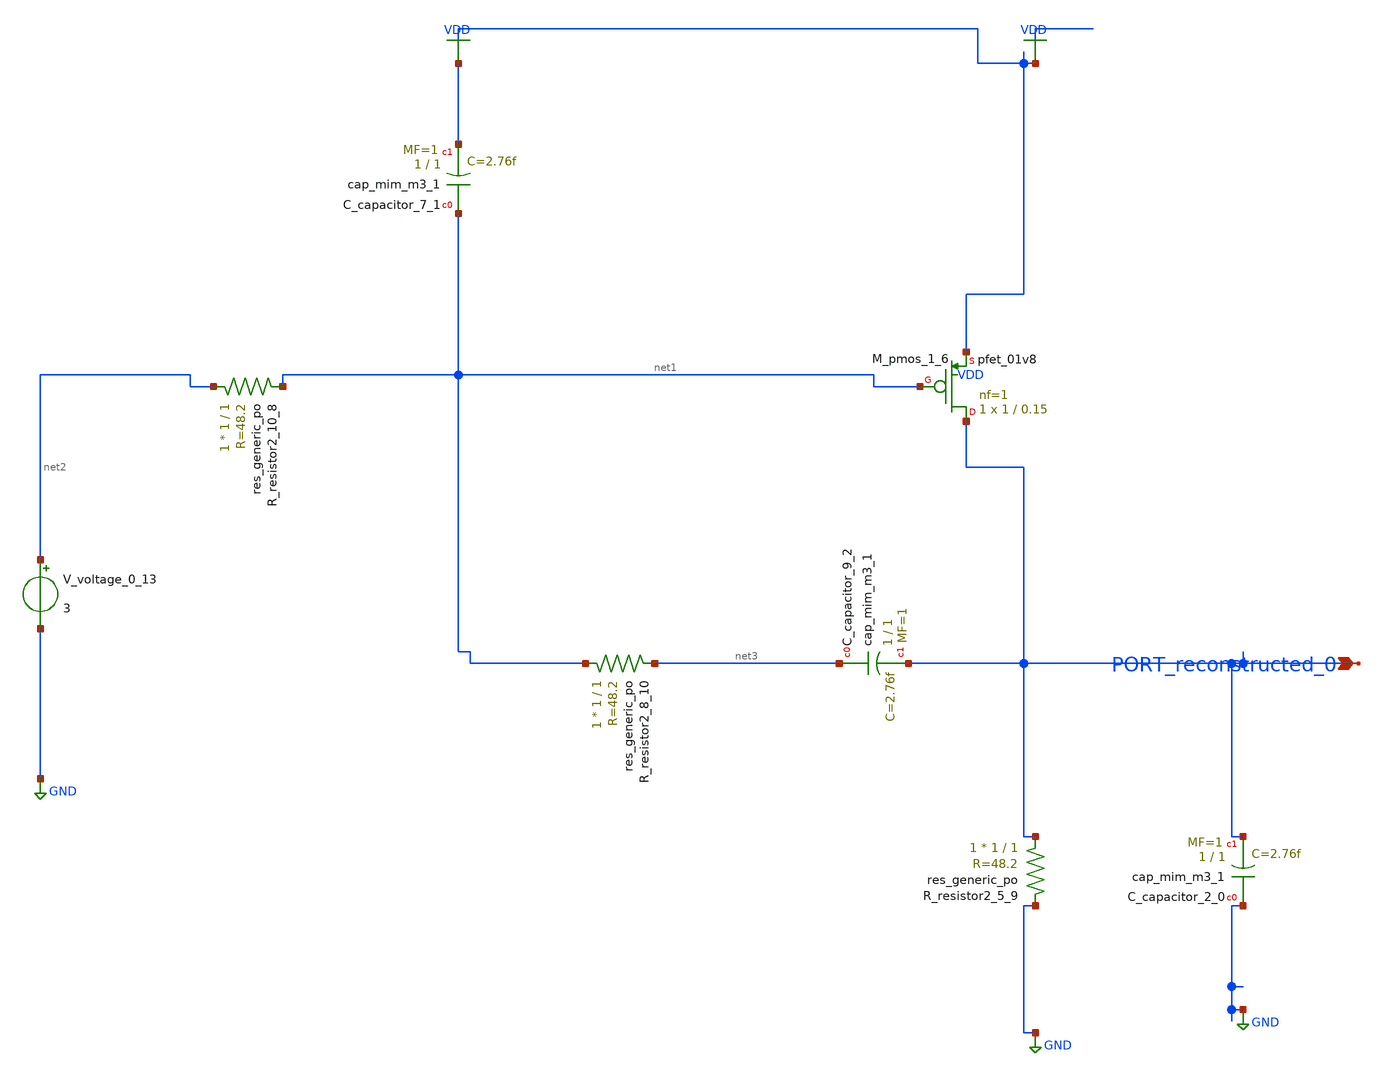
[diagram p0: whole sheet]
** sch_path: schematics/AMSNet/724.sch
**.subckt 724 PORT_reconstructed_0
*.ipin PORT_reconstructed_0
XC_capacitor_2_0 GND PORT_reconstructed_0 sky130_fd_pr__cap_mim_m3_1 W=1 L=1 MF=1 m=1
XC_capacitor_7_1 net1 VDD sky130_fd_pr__cap_mim_m3_1 W=1 L=1 MF=1 m=1
XC_capacitor_9_2 net3 PORT_reconstructed_0 sky130_fd_pr__cap_mim_m3_1 W=1 L=1 MF=1 m=1
XM_pmos_1_6 PORT_reconstructed_0 net1 VDD VDD sky130_fd_pr__pfet_01v8 L=0.15 W=1 nf=1 ad='int((1 + 1)/2) * 1 / 1 * 0.29'
+ as='int((1 + 2)/2) * 1 / 1 * 0.29' pd='2*int((1 + 1)/2) * (1 / 1 + 0.29)' ps='2*int((1 + 2)/2) * (1 / 1 + 0.29)'
+ nrd='0.29 / 1 ' nrs='0.29 / 1 ' sa=0 sb=0 sd=0 mult=1 m=1
XR_resistor2_10_8 net2 net1 sky130_fd_pr__res_generic_po W=1 L=1 m=1
XR_resistor2_5_9 PORT_reconstructed_0 GND sky130_fd_pr__res_generic_po W=1 L=1 m=1
XR_resistor2_8_10 net1 net3 sky130_fd_pr__res_generic_po W=1 L=1 m=1
V_voltage_0_13 net2 GND 3
**.ends
.GLOBAL GND
.GLOBAL VDD
.end
